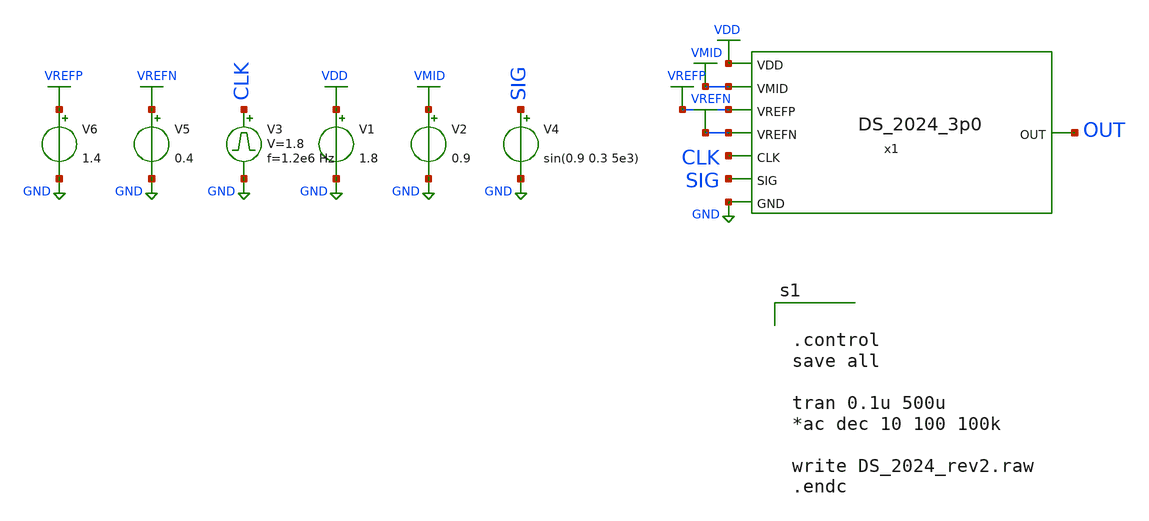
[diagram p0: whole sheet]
** sch_path: SP24_caravel_user_project_analog/xschem/xschem_DeltaSigma/DS_2024_Bench.sch
.lib $::SKYWATER_MODELS/sky130.lib.spice tt
.include $::SKYWATER_STDCELLS/sky130_fd_sc_hd.spice

**.subckt DS_2024_Bench
V1 VDD GND 1.8
V2 VMID GND 0.9
V3 CLK GND pulse 0 1.8 '0.495/ 1.2e6 ' '0.01/1.2e6 ' '0.01/1.2e6 ' '0.49/1.2e6 ' '1/1.2e6 '
V4 SIG GND sin(0.9 0.3 5e3)
V5 VREFN GND 0.4
V6 VREFP GND 1.4
x1 VDD VMID OUT VREFP VREFN GND SIG CLK DS_2024_3p0
**** begin user architecture code


.control
save all

tran 0.1u 500u
*ac dec 10 100 100k

write DS_2024_rev2.raw
.endc


**** end user architecture code
**.ends
.GLOBAL VDD
.GLOBAL GND
.GLOBAL VMID
.GLOBAL VREFN
.GLOBAL VREFP
.end
